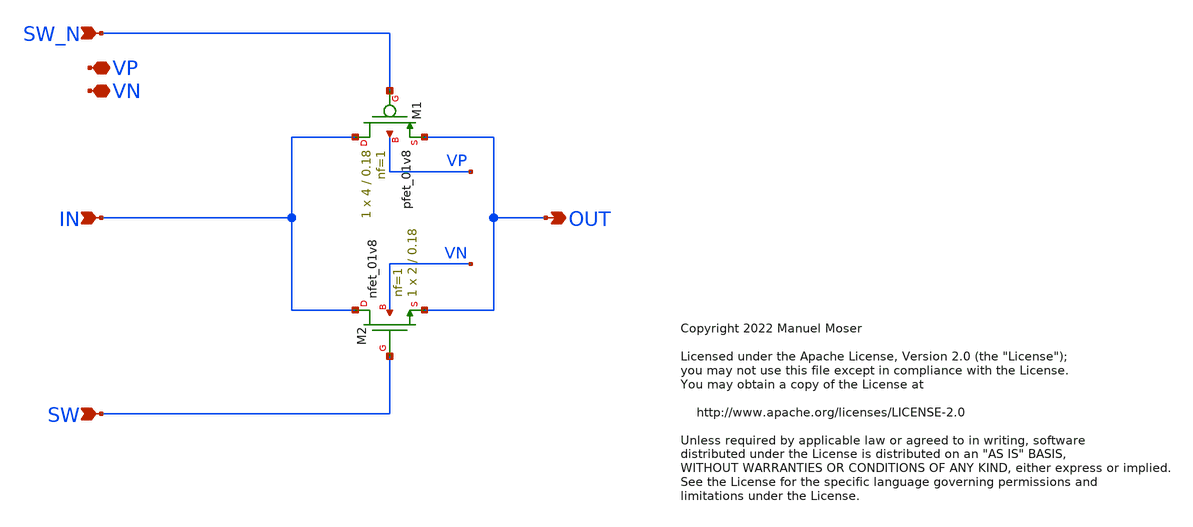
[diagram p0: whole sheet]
** sch_path: xschem/archive/180n_legacy/switch_180n/switch_180n.sch
* Copyright 2022 Manuel Moser
* Licensed under the Apache License, Version 2.0 (the "License");
**.subckt switch_180n VN VP IN OUT SW_N SW
*.iopin VN
*.iopin VP
*.ipin IN
*.opin OUT
*.ipin SW_N
*.ipin SW
XM1 IN SW_N OUT VP sky130_fd_pr__pfet_01v8 L=0.18 W=4 nf=1 ad='int((nf+1)/2) * W/nf * 0.29' as='int((nf+2)/2) * W/nf * 0.29'
+ pd='2*int((nf+1)/2) * (W/nf + 0.29)' ps='2*int((nf+2)/2) * (W/nf + 0.29)' nrd='0.29 / W' nrs='0.29 / W'
+ sa=0 sb=0 sd=0 mult=1 m=1
XM2 IN SW OUT VN sky130_fd_pr__nfet_01v8 L=0.18 W=2 nf=1 ad='int((nf+1)/2) * W/nf * 0.29' as='int((nf+2)/2) * W/nf * 0.29'
+ pd='2*int((nf+1)/2) * (W/nf + 0.29)' ps='2*int((nf+2)/2) * (W/nf + 0.29)' nrd='0.29 / W' nrs='0.29 / W'
+ sa=0 sb=0 sd=0 mult=1 m=1
**.ends
.end
